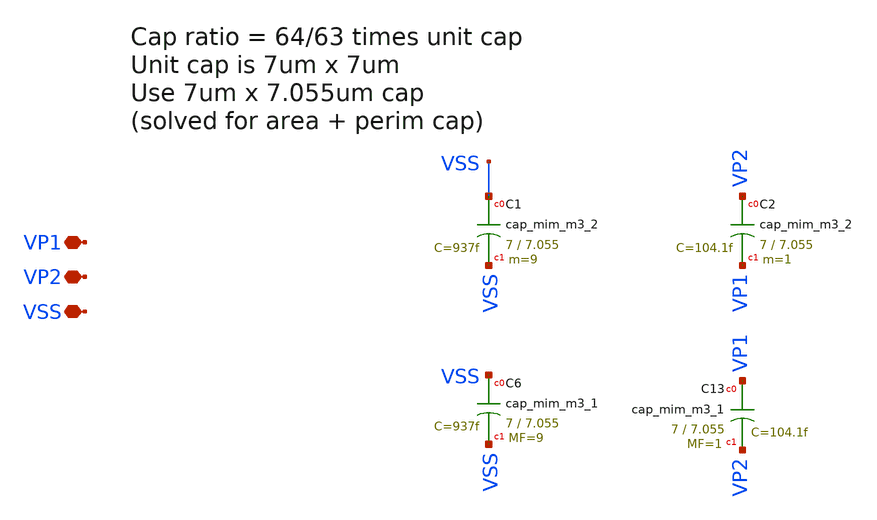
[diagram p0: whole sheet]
** sch_path: xschem/EF_SC_CAP.sch
**.subckt EF_SC_CAP VP1 VP2 VSS
*.iopin VP1
*.iopin VP2
*.iopin VSS
XC13 VP1 VP2 sky130_fd_pr__cap_mim_m3_1 W=7 L=7.055 MF=1 m=1
XC6 VSS VSS sky130_fd_pr__cap_mim_m3_1 W=7 L=7.055 MF=9 m=9
XC1 VSS VSS sky130_fd_pr__cap_mim_m3_2 W=7 L=7.055 MF=9 m=9
XC2 VP2 VP1 sky130_fd_pr__cap_mim_m3_2 W=7 L=7.055 MF=1 m=1
**.ends
.end
